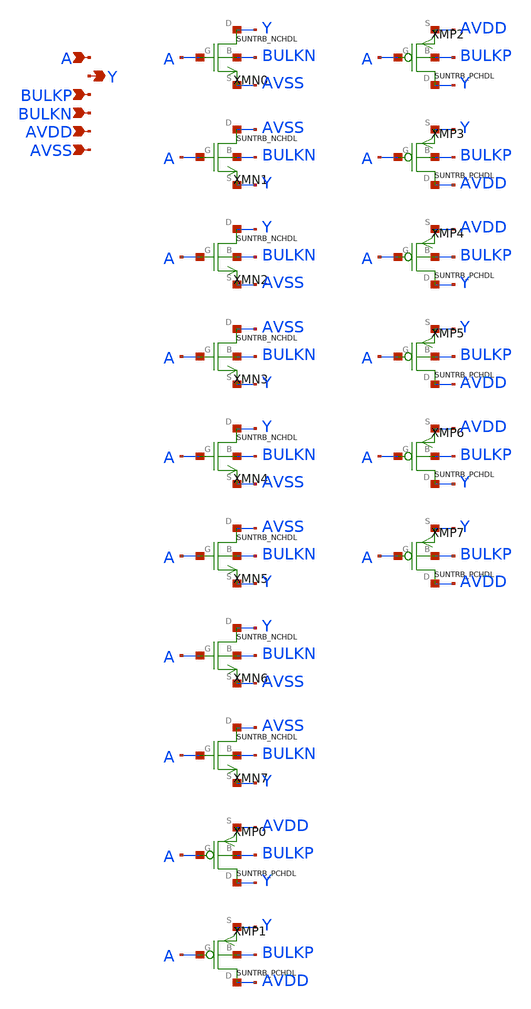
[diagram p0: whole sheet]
** sch_path: ip/sun_trb_sky130nm/design/SUN_TRB_SKY130NM/SUNTRB_IVX8_CV.sch
**.subckt SUNTRB_IVX8_CV A Y BULKP BULKN AVDD AVSS
*.ipin A
*.opin Y
*.ipin BULKP
*.ipin BULKN
*.ipin AVDD
*.ipin AVSS
XMN0 Y A AVSS BULKN SUNTRB_NCHDL xoffset=0 yoffset=0 angle=0
XMN1 AVSS A Y BULKN SUNTRB_NCHDL xoffset=0 yoffset=0 angle=0
XMN2 Y A AVSS BULKN SUNTRB_NCHDL xoffset=0 yoffset=0 angle=0
XMN3 AVSS A Y BULKN SUNTRB_NCHDL xoffset=0 yoffset=0 angle=0
XMN4 Y A AVSS BULKN SUNTRB_NCHDL xoffset=0 yoffset=0 angle=0
XMN5 AVSS A Y BULKN SUNTRB_NCHDL xoffset=0 yoffset=0 angle=0
XMN6 Y A AVSS BULKN SUNTRB_NCHDL xoffset=0 yoffset=0 angle=0
XMN7 AVSS A Y BULKN SUNTRB_NCHDL xoffset=0 yoffset=0 angle=0
XMP0 Y A AVDD BULKP SUNTRB_PCHDL
XMP1 AVDD A Y BULKP SUNTRB_PCHDL
XMP2 Y A AVDD BULKP SUNTRB_PCHDL
XMP3 AVDD A Y BULKP SUNTRB_PCHDL
XMP4 Y A AVDD BULKP SUNTRB_PCHDL
XMP5 AVDD A Y BULKP SUNTRB_PCHDL
XMP6 Y A AVDD BULKP SUNTRB_PCHDL
XMP7 AVDD A Y BULKP SUNTRB_PCHDL
**.ends
.end
